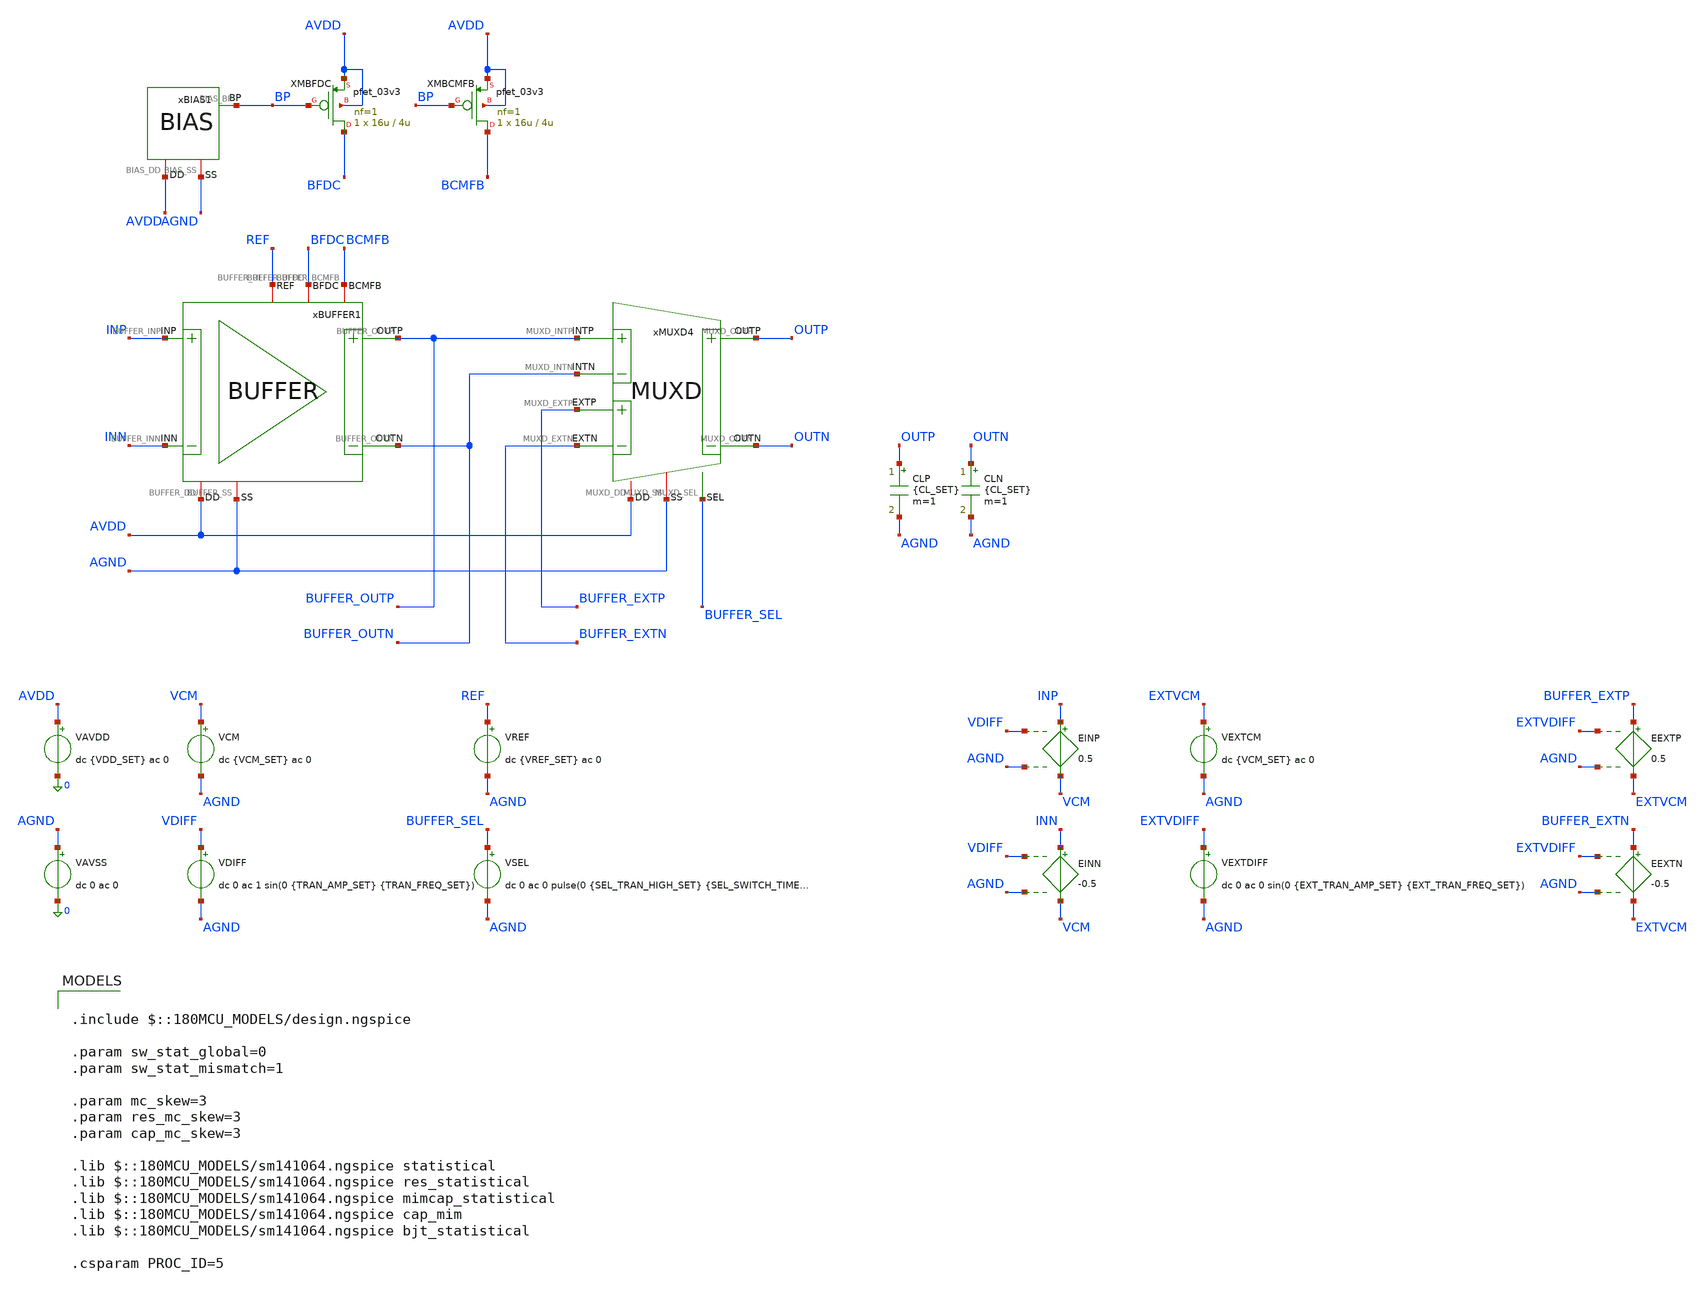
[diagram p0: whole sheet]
** sch_path: Design_Files/IC Design/Testbench/AFE_BLOCKS/BUFFER/BUFFER_TB_MM.sch
**.subckt BUFFER_TB_MM
CLP OUTP AGND {CL_SET} m=1
CLN OUTN AGND {CL_SET} m=1
xBIAS1 AVDD AGND BP BIAS
XMBFDC BFDC BP AVDD AVDD pfet_03v3 L=4u W=16u nf=1 ad='int((nf+1)/2) * W/nf * 0.18u' as='int((nf+2)/2) * W/nf * 0.18u'
+ pd='2*int((nf+1)/2) * (W/nf + 0.18u)' ps='2*int((nf+2)/2) * (W/nf + 0.18u)' nrd='0.18u / W' nrs='0.18u / W'
+ sa=0 sb=0 sd=0 m=1
XMBCMFB BCMFB BP AVDD AVDD pfet_03v3 L=4u W=16u nf=1 ad='int((nf+1)/2) * W/nf * 0.18u' as='int((nf+2)/2) * W/nf * 0.18u'
+ pd='2*int((nf+1)/2) * (W/nf + 0.18u)' ps='2*int((nf+2)/2) * (W/nf + 0.18u)' nrd='0.18u / W' nrs='0.18u / W'
+ sa=0 sb=0 sd=0 m=1
VAVDD AVDD 0 dc {VDD_SET} ac 0
.save i(vavdd)
VAVSS AGND 0 dc 0 ac 0
VCM VCM AGND dc {VCM_SET} ac 0
VDIFF VDIFF AGND dc 0 ac 1 sin(0 {TRAN_AMP_SET} {TRAN_FREQ_SET})
VREF REF AGND dc {VREF_SET} ac 0
VSEL BUFFER_SEL AGND dc 0 ac 0 pulse(0 {SEL_TRAN_HIGH_SET} {SEL_SWITCH_TIME_SET} 1u 1u 400m 800m)
VEXTCM EXTVCM AGND dc {VCM_SET} ac 0
VEXTDIFF EXTVDIFF AGND dc 0 ac 0 sin(0 {EXT_TRAN_AMP_SET} {EXT_TRAN_FREQ_SET})
EINP INP VCM VDIFF AGND 0.5
EINN INN VCM VDIFF AGND -0.5
EEXTP BUFFER_EXTP EXTVCM EXTVDIFF AGND 0.5
EEXTN BUFFER_EXTN EXTVCM EXTVDIFF AGND -0.5
xMUXD4 AVDD AGND BUFFER_OUTP BUFFER_OUTN OUTN OUTP BUFFER_EXTP BUFFER_EXTN BUFFER_SEL MUXD
xBUFFER1 AVDD AGND INP INN BUFFER_OUTN BFDC BUFFER_OUTP BCMFB REF BUFFER
**** begin user architecture code

.include $::180MCU_MODELS/design.ngspice

.param sw_stat_global=0
.param sw_stat_mismatch=1

.param mc_skew=3
.param res_mc_skew=3
.param cap_mc_skew=3

.lib $::180MCU_MODELS/sm141064.ngspice statistical
.lib $::180MCU_MODELS/sm141064.ngspice res_statistical
.lib $::180MCU_MODELS/sm141064.ngspice mimcap_statistical
.lib $::180MCU_MODELS/sm141064.ngspice cap_mim
.lib $::180MCU_MODELS/sm141064.ngspice bjt_statistical

.csparam PROC_ID=5



.param VDD_SET=3.3
.param TEMP_SET=27

.param VCM_SET={VDD_SET/2}
.param VREF_SET={VDD_SET/2}

.param CL_SET=10p

.param BUFFER_GAIN_TARGET_SET=1

.param TRAN_AMP_SET=50m
.param TRAN_FREQ_SET=10

.param EXT_TRAN_AMP_SET=0
.param EXT_TRAN_FREQ_SET=25

.param SEL_TRAN_HIGH_SET=0
.param SEL_SWITCH_TIME_SET=200m

.csparam MC_RUNS=200

.temp {TEMP_SET}

.options gmin=1e-12
.options rshunt=1e12
.options method=gear





.control

destroy all

set noaskquit
set wr_singlescale
unset wr_vecnames

option klu
option numdgt=15
option method=gear
option maxord=2
option plotwinsize=0

if $&PROC_ID = 5
set mode=MM
set tag=mm
else
if $&PROC_ID = 6
set mode=GL
set tag=gl
else
set mode=FULL
set tag=full
end
end

alterparam VDD_SET=3.3
alterparam TEMP_SET=27
alterparam SEL_TRAN_HIGH_SET=0
alterparam EXT_TRAN_AMP_SET=0

reset

shell mkdir -p /foss/designs/ECG_Acquisition_IC/Measurement_Results/IC_Simulation/AFE_BLOCKS/BUFFER/{$mode}.Result_txt
shell rm -f /foss/designs/ECG_Acquisition_IC/Measurement_Results/IC_Simulation/AFE_BLOCKS/BUFFER/{$mode}.Result_txt/{$tag}.*_mc_summary.txt

let run=1

dowhile run <= $&MC_RUNS

setseed $&run
mc_source

save all
save @m.xmbfdc.m0[id]
save @m.xmbcmfb.m0[id]

alter @VAVDD[DC]=3.3
alter @VAVSS[DC]=0

alter @VCM[DC]=1.65
alter @VREF[DC]=1.65

alter @VSEL[DC]=0
alter @VDIFF[DC]=0

alter @VAVDD[ACMAG]=0
alter @VAVSS[ACMAG]=0
alter @VCM[ACMAG]=0
alter @VREF[ACMAG]=0
alter @VDIFF[ACMAG]=0
alter @VEXTDIFF[ACMAG]=0


* OFFSET

dc VDIFF -20m 20m 10u

let buffer_diff=v(BUFFER_OUTP)-v(BUFFER_OUTN)

meas dc vos_meas when buffer_diff=0 cross=1

set vos_val=$&vos_meas

destroy all

alter @VDIFF[DC]=$vos_val


* OP

op

let buffer_out_cm=0.5*(v(BUFFER_OUTP)+v(BUFFER_OUTN))-v(AGND)
let out_cm_error=buffer_out_cm-v(REF)

let idd_total=abs(vavdd#branch)
let power_total=(v(AVDD)-v(AGND))*idd_total

let ibfdc=abs(@m.xmbfdc.m0[id])
let ibcmfb=abs(@m.xmbcmfb.m0[id])

set idd_val=$&idd_total
set power_val=$&power_total
set outcmerr_val=$&out_cm_error
set ibfdc_val=$&ibfdc
set ibcmfb_val=$&ibcmfb

destroy all


* DIFF AC

alter @VDIFF[ACMAG]=1
alter @VCM[ACMAG]=0
alter @VREF[ACMAG]=0
alter @VEXTDIFF[ACMAG]=0
alter @VAVDD[ACMAG]=0
alter @VAVSS[ACMAG]=0

ac dec 150 0.01 100Meg

let vin_diff=v(INP)-v(INN)
let buffer_diff=v(BUFFER_OUTP)-v(BUFFER_OUTN)

let buffer_gain=mag(buffer_diff/vin_diff)

meas ac gain10 find buffer_gain at=10
meas ac gain150 find buffer_gain at=150

let norm_db=20*log10(buffer_gain/$&gain10)

meas ac bw3db when norm_db=-3 fall=1

meas ac ad60 find buffer_gain at=60
meas ac ad150 find buffer_gain at=150

let gain_error_pct=100*($&gain10/$&BUFFER_GAIN_TARGET_SET-1)

set gain10_val=$&gain10
set gain150_val=$&gain150
set gainerr_val=$&gain_error_pct
set bw3db_val=$&bw3db

set ad60_val=$&ad60
set ad150_val=$&ad150

destroy all


* CMRR

alter @VDIFF[ACMAG]=0
alter @VCM[ACMAG]=1
alter @VREF[ACMAG]=0
alter @VEXTDIFF[ACMAG]=0
alter @VAVDD[ACMAG]=0
alter @VAVSS[ACMAG]=0

ac dec 100 10 1k

let vin_cm=0.5*(v(INP)+v(INN))-v(AGND)
let buffer_diff=v(BUFFER_OUTP)-v(BUFFER_OUTN)

let acm=mag(buffer_diff/vin_cm)

meas ac acm60 find acm at=60
meas ac acm150 find acm at=150

let cmrr60=20*log10($ad60_val/$&acm60)
let cmrr150=20*log10($ad150_val/$&acm150)

set cmrr60_val=$&cmrr60
set cmrr150_val=$&cmrr150

destroy all


* SUMMARY

echo $&run $ibfdc_val $ibcmfb_val $idd_val $power_val $outcmerr_val $vos_val $gain10_val $gainerr_val
+ $gain150_val $bw3db_val $cmrr60_val $cmrr150_val >> /foss/designs/ECG_Acquisition_IC/Measurement_Results/IC_Simulation/AFE_BLOCKS/BUFFER/{$mode}.Result_txt/{$tag}.buffer_mc_summary.txt

let run=run+1

end

quit

.endc



**** end user architecture code
**.ends
.end
